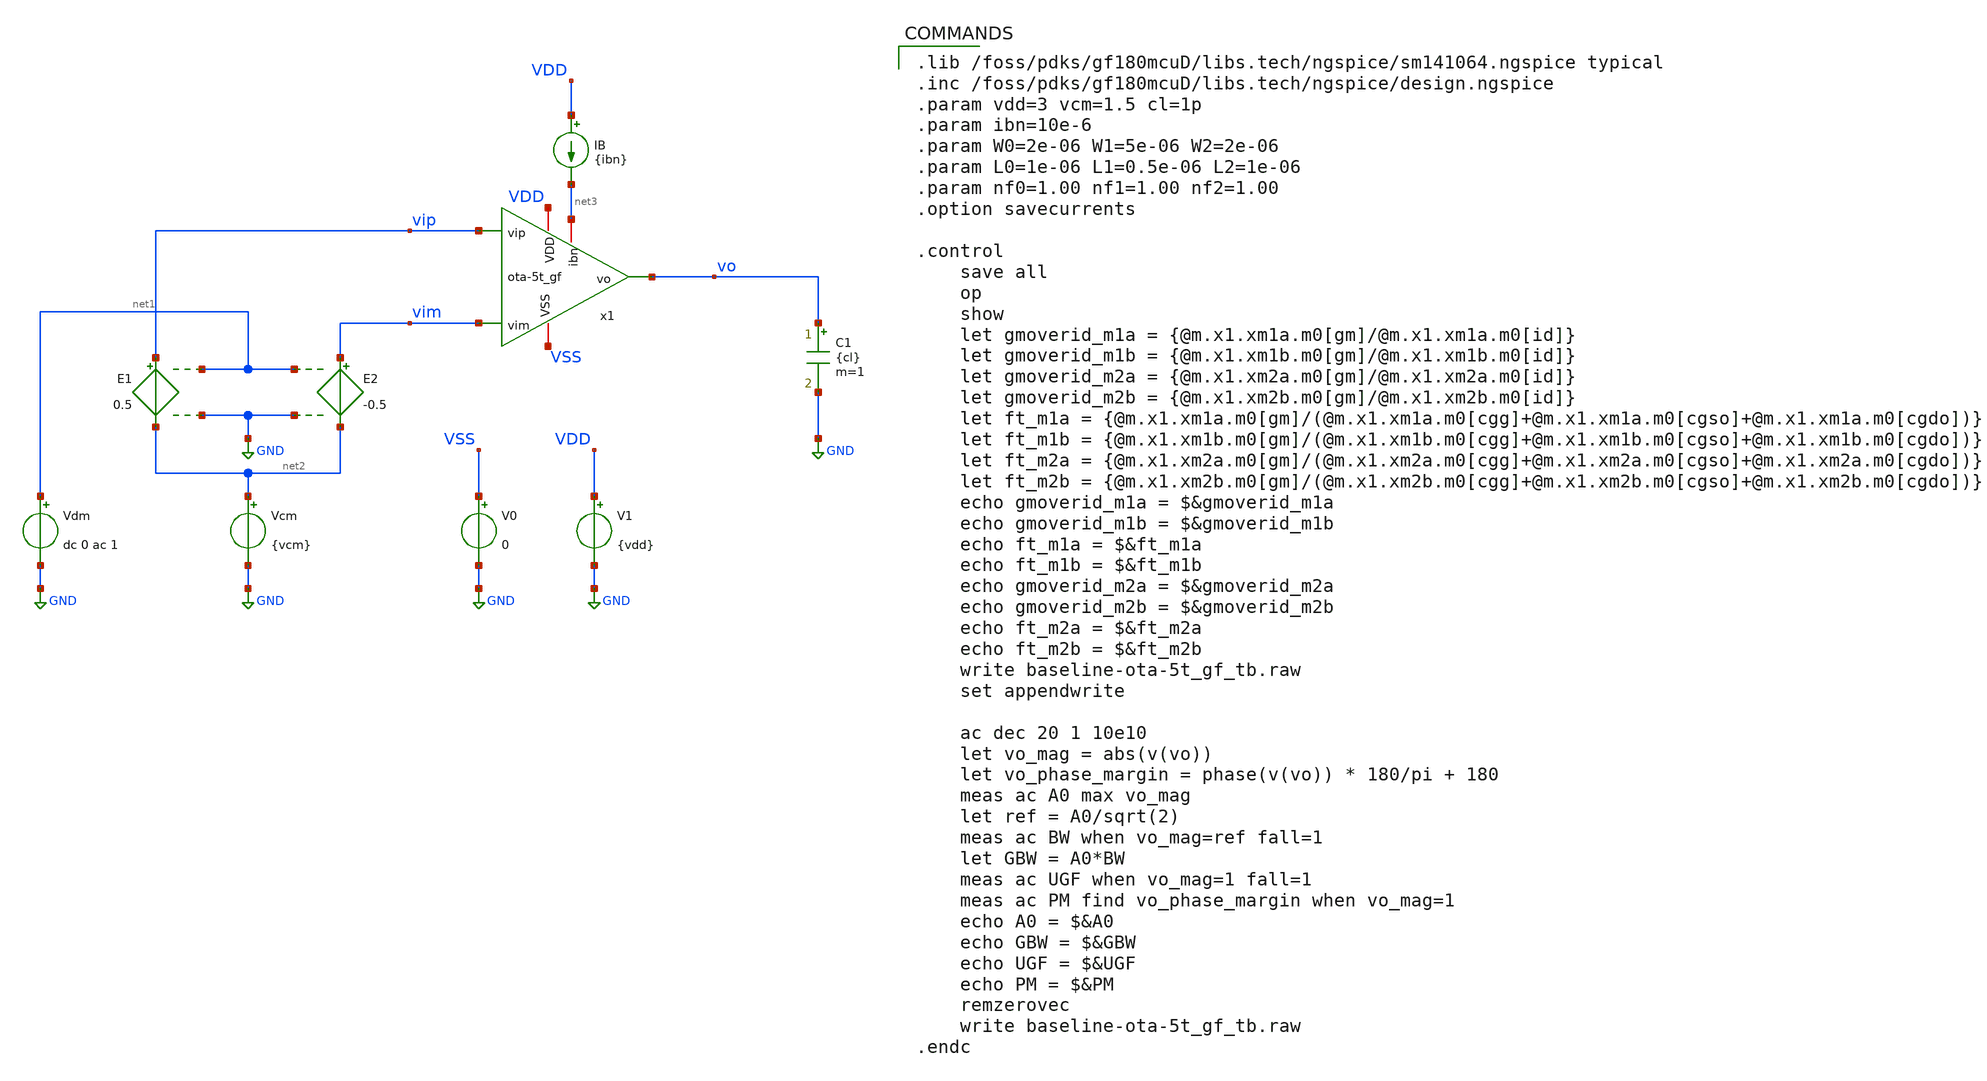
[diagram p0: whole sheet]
** sch_path: gf180-2025/ota/baseline-ota-5t_gf_tb.sch
**.subckt baseline-ota-5t_gf_tb
E1 vip net2 net1 GND 0.5
E2 vim net2 net1 GND -0.5
Vdm net1 GND dc 0 ac 1
Vcm net2 GND {vcm}
V0 VSS GND 0
V1 VDD GND {vdd}
C1 vo GND {cl} m=1
IB VDD net3 {ibn}
x1 vip vim vo VDD VSS net3 ota-5t_gf
**** begin user architecture code

.lib /foss/pdks/gf180mcuD/libs.tech/ngspice/sm141064.ngspice typical
.inc /foss/pdks/gf180mcuD/libs.tech/ngspice/design.ngspice
.param vdd=3 vcm=1.5 cl=1p
.param ibn=10e-6
.param W0=2e-06 W1=5e-06 W2=2e-06
.param L0=1e-06 L1=0.5e-06 L2=1e-06
.param nf0=1.00 nf1=1.00 nf2=1.00
.option savecurrents

.control
    save all
    op
    show
    let gmoverid_m1a = {@m.x1.xm1a.m0[gm]/@m.x1.xm1a.m0[id]}
    let gmoverid_m1b = {@m.x1.xm1b.m0[gm]/@m.x1.xm1b.m0[id]}
    let gmoverid_m2a = {@m.x1.xm2a.m0[gm]/@m.x1.xm2a.m0[id]}
    let gmoverid_m2b = {@m.x1.xm2b.m0[gm]/@m.x1.xm2b.m0[id]}
    let ft_m1a = {@m.x1.xm1a.m0[gm]/(@m.x1.xm1a.m0[cgg]+@m.x1.xm1a.m0[cgso]+@m.x1.xm1a.m0[cgdo])}
    let ft_m1b = {@m.x1.xm1b.m0[gm]/(@m.x1.xm1b.m0[cgg]+@m.x1.xm1b.m0[cgso]+@m.x1.xm1b.m0[cgdo])}
    let ft_m2a = {@m.x1.xm2a.m0[gm]/(@m.x1.xm2a.m0[cgg]+@m.x1.xm2a.m0[cgso]+@m.x1.xm2a.m0[cgdo])}
    let ft_m2b = {@m.x1.xm2b.m0[gm]/(@m.x1.xm2b.m0[cgg]+@m.x1.xm2b.m0[cgso]+@m.x1.xm2b.m0[cgdo])}
    echo gmoverid_m1a = $&gmoverid_m1a
    echo gmoverid_m1b = $&gmoverid_m1b
    echo ft_m1a = $&ft_m1a
    echo ft_m1b = $&ft_m1b
    echo gmoverid_m2a = $&gmoverid_m2a
    echo gmoverid_m2b = $&gmoverid_m2b
    echo ft_m2a = $&ft_m2a
    echo ft_m2b = $&ft_m2b
    write baseline-ota-5t_gf_tb.raw
    set appendwrite

    ac dec 20 1 10e10
    let vo_mag = abs(v(vo))
    let vo_phase_margin = phase(v(vo)) * 180/pi + 180
    meas ac A0 max vo_mag
    let ref = A0/sqrt(2)
    meas ac BW when vo_mag=ref fall=1
    let GBW = A0*BW
    meas ac UGF when vo_mag=1 fall=1
    meas ac PM find vo_phase_margin when vo_mag=1
    echo A0 = $&A0
    echo GBW = $&GBW
    echo UGF = $&UGF
    echo PM = $&PM
    remzerovec
    write baseline-ota-5t_gf_tb.raw
.endc


**** end user architecture code
**.ends

* expanding   symbol:  ota-5t_gf.sym # of pins=6
** sym_path: ota-5t_gf.sym
** sch_path: ota-5t_gf.sch
.subckt ota-5t_gf vip vim vo VDD VSS ibn
*.ipin vip
*.ipin vim
*.opin vo
*.iopin VDD
*.iopin VSS
*.iopin ibn
XM2b vo vmirr VDD VDD pfet_03v3 L={L2} W={W2} nf={nf2} ad='int((nf+1)/2) * W/nf * 0.18u' as='int((nf+2)/2) * W/nf * 0.18u'
+ pd='2*int((nf+1)/2) * (W/nf + 0.18u)' ps='2*int((nf+2)/2) * (W/nf + 0.18u)' nrd='0.18u / W' nrs='0.18u / W'
+ sa=0 sb=0 sd=0 m=1
XM2a vmirr vmirr VDD VDD pfet_03v3 L={L2} W={W2} nf={nf2} ad='int((nf+1)/2) * W/nf * 0.18u' as='int((nf+2)/2) * W/nf * 0.18u'
+ pd='2*int((nf+1)/2) * (W/nf + 0.18u)' ps='2*int((nf+2)/2) * (W/nf + 0.18u)' nrd='0.18u / W' nrs='0.18u / W'
+ sa=0 sb=0 sd=0 m=1
XM1a vmirr vip vtail VSS nfet_03v3 L={L1} W={W1} nf={nf1} ad='int((nf+1)/2) * W/nf * 0.18u' as='int((nf+2)/2) * W/nf * 0.18u'
+ pd='2*int((nf+1)/2) * (W/nf + 0.18u)' ps='2*int((nf+2)/2) * (W/nf + 0.18u)' nrd='0.18u / W' nrs='0.18u / W'
+ sa=0 sb=0 sd=0 m=1
XM0b vtail ibn VSS VSS nfet_03v3 L={L0} W={W0} nf={nf0} ad='int((nf+1)/2) * W/nf * 0.18u' as='int((nf+2)/2) * W/nf * 0.18u'
+ pd='2*int((nf+1)/2) * (W/nf + 0.18u)' ps='2*int((nf+2)/2) * (W/nf + 0.18u)' nrd='0.18u / W' nrs='0.18u / W'
+ sa=0 sb=0 sd=0 m=1
XM1b vo vim vtail VSS nfet_03v3 L={L1} W={W1} nf={nf1} ad='int((nf+1)/2) * W/nf * 0.18u' as='int((nf+2)/2) * W/nf * 0.18u'
+ pd='2*int((nf+1)/2) * (W/nf + 0.18u)' ps='2*int((nf+2)/2) * (W/nf + 0.18u)' nrd='0.18u / W' nrs='0.18u / W'
+ sa=0 sb=0 sd=0 m=1
XM0a ibn ibn VSS VSS nfet_03v3 L={L0} W={W0} nf={nf0} ad='int((nf+1)/2) * W/nf * 0.18u' as='int((nf+2)/2) * W/nf * 0.18u'
+ pd='2*int((nf+1)/2) * (W/nf + 0.18u)' ps='2*int((nf+2)/2) * (W/nf + 0.18u)' nrd='0.18u / W' nrs='0.18u / W'
+ sa=0 sb=0 sd=0 m=1
.ends

.GLOBAL GND
.end
